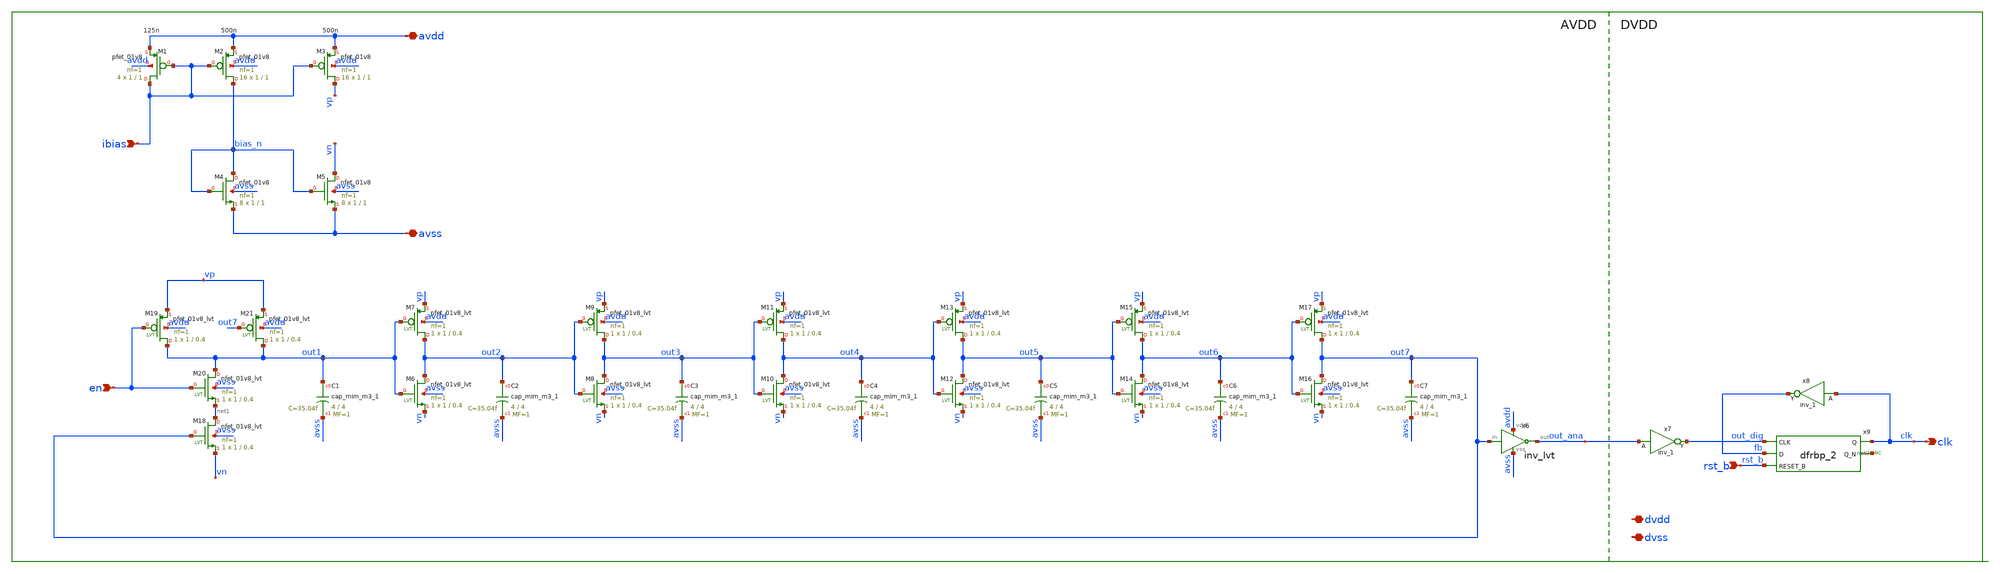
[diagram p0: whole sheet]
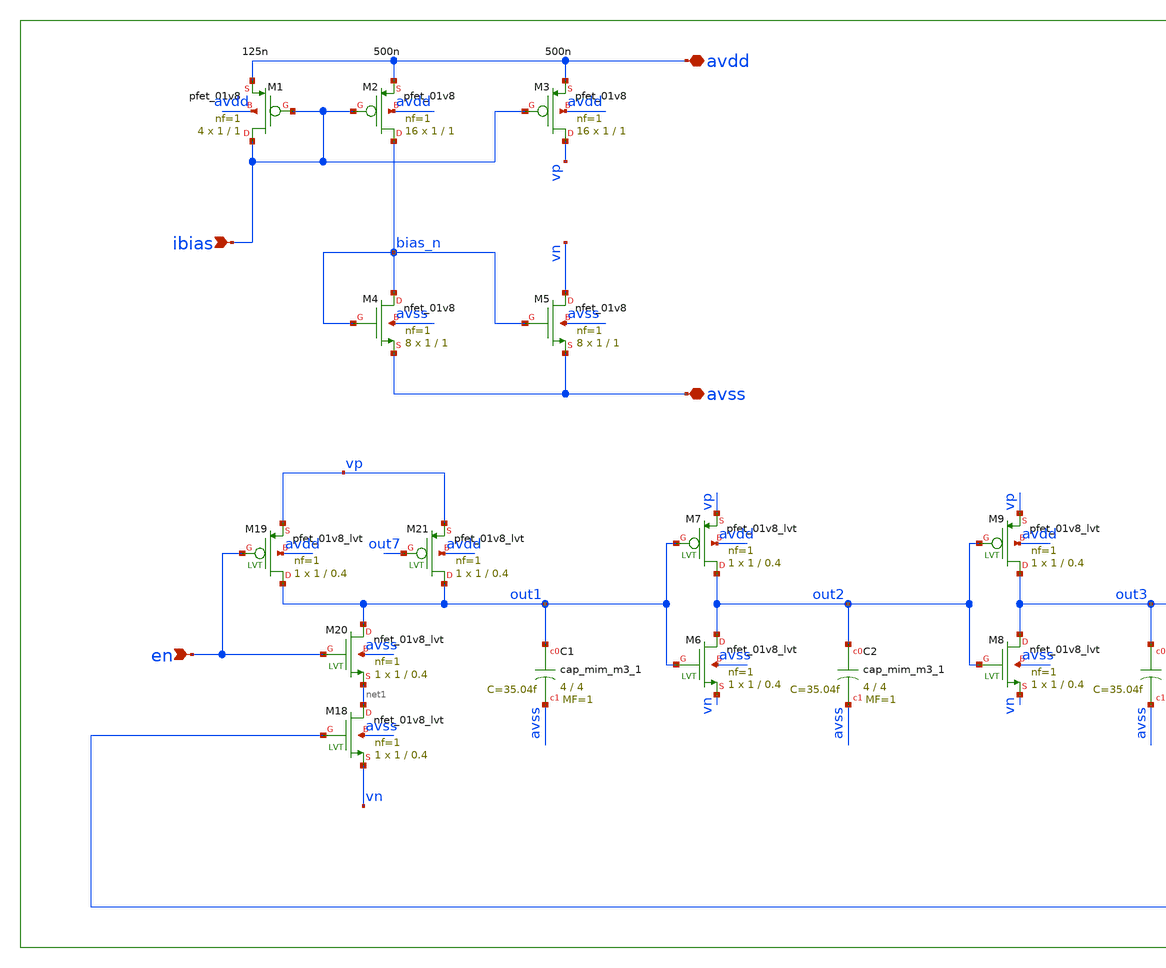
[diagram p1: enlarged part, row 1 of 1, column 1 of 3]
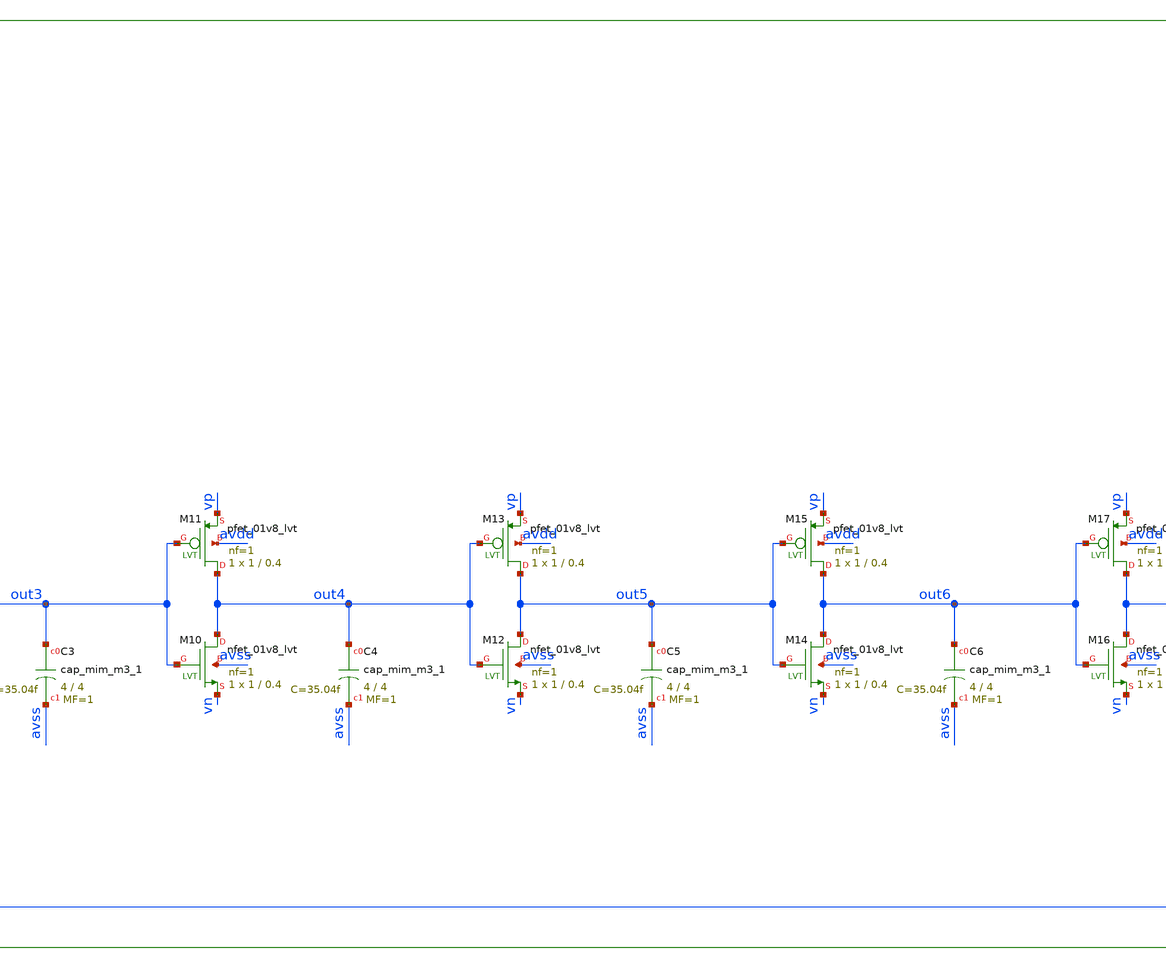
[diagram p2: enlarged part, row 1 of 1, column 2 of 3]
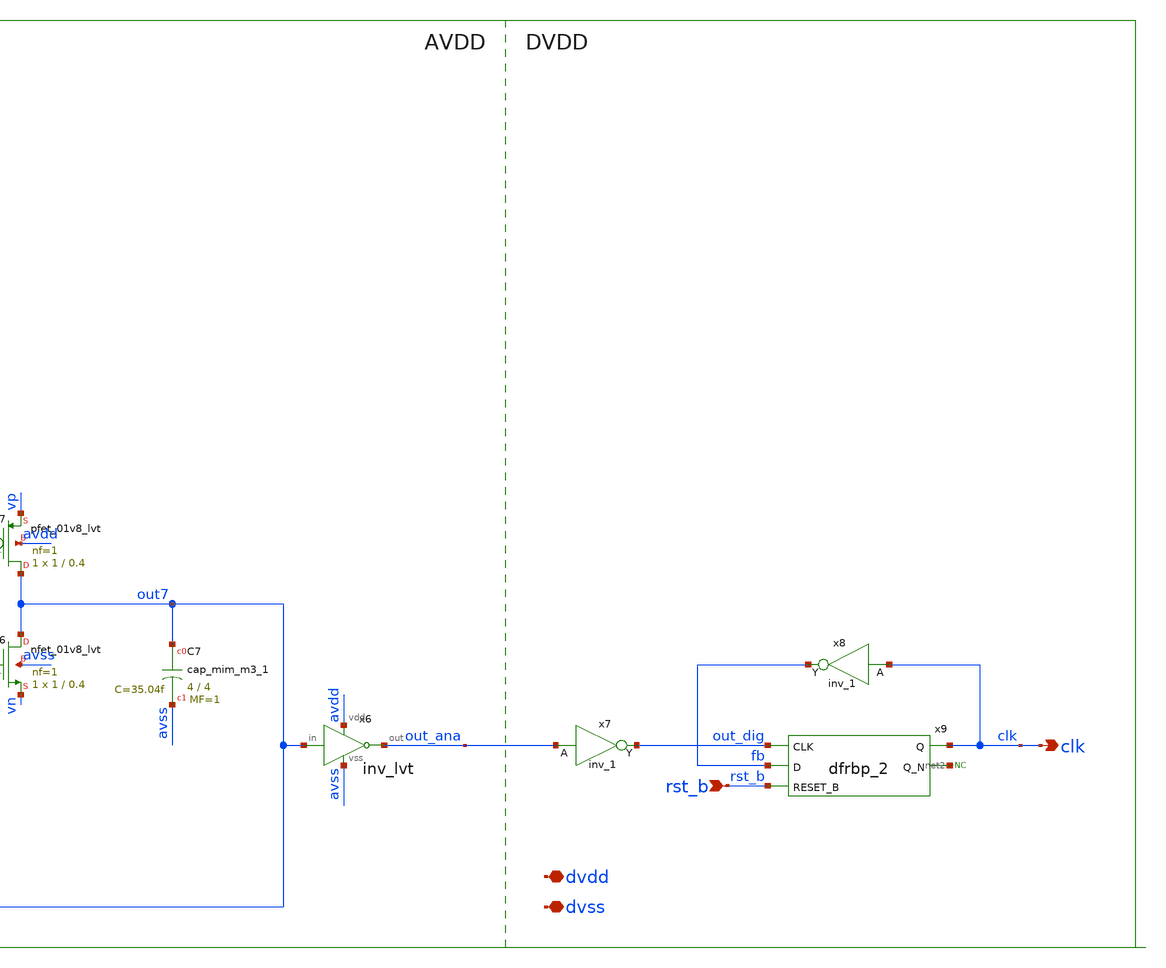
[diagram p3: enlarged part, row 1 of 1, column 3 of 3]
** sch_path: xschem/rosc/rosc.sch
**.subckt rosc en avss clk dvdd dvss avdd rst_b ibias
*.ipin en
*.iopin avss
*.opin clk
*.iopin dvdd
*.iopin dvss
*.iopin avdd
*.ipin rst_b
*.ipin ibias
x8 clk dvss dvss dvdd dvdd fb sky130_fd_sc_hd__inv_1
* noconn #net2
XM2 bias_n ibias avdd avdd sky130_fd_pr__pfet_01v8 L=1 W=1 nf=1 ad='int((nf+1)/2) * W/nf * 0.29' as='int((nf+2)/2) * W/nf * 0.29'
+ pd='2*int((nf+1)/2) * (W/nf + 0.29)' ps='2*int((nf+2)/2) * (W/nf + 0.29)' nrd='0.29 / W' nrs='0.29 / W'
+ sa=0 sb=0 sd=0 mult=16 m=16
XM1 ibias ibias avdd avdd sky130_fd_pr__pfet_01v8 L=1 W=1 nf=1 ad='int((nf+1)/2) * W/nf * 0.29' as='int((nf+2)/2) * W/nf * 0.29'
+ pd='2*int((nf+1)/2) * (W/nf + 0.29)' ps='2*int((nf+2)/2) * (W/nf + 0.29)' nrd='0.29 / W' nrs='0.29 / W'
+ sa=0 sb=0 sd=0 mult=4 m=4
x9 out_dig fb rst_b dvss dvss dvdd dvdd clk net2 sky130_fd_sc_hd__dfrbp_2
XM4 bias_n bias_n avss avss sky130_fd_pr__nfet_01v8 L=1 W=1 nf=1 ad='int((nf+1)/2) * W/nf * 0.29' as='int((nf+2)/2) * W/nf * 0.29'
+ pd='2*int((nf+1)/2) * (W/nf + 0.29)' ps='2*int((nf+2)/2) * (W/nf + 0.29)' nrd='0.29 / W' nrs='0.29 / W'
+ sa=0 sb=0 sd=0 mult=8 m=8
XM5 vn bias_n avss avss sky130_fd_pr__nfet_01v8 L=1 W=1 nf=1 ad='int((nf+1)/2) * W/nf * 0.29' as='int((nf+2)/2) * W/nf * 0.29'
+ pd='2*int((nf+1)/2) * (W/nf + 0.29)' ps='2*int((nf+2)/2) * (W/nf + 0.29)' nrd='0.29 / W' nrs='0.29 / W'
+ sa=0 sb=0 sd=0 mult=8 m=8
x7 out_ana dvss dvss dvdd dvdd out_dig sky130_fd_sc_hd__inv_1
XM3 vp ibias avdd avdd sky130_fd_pr__pfet_01v8 L=1 W=1 nf=1 ad='int((nf+1)/2) * W/nf * 0.29' as='int((nf+2)/2) * W/nf * 0.29'
+ pd='2*int((nf+1)/2) * (W/nf + 0.29)' ps='2*int((nf+2)/2) * (W/nf + 0.29)' nrd='0.29 / W' nrs='0.29 / W'
+ sa=0 sb=0 sd=0 mult=16 m=16
XC1 out1 avss sky130_fd_pr__cap_mim_m3_1 W=4 L=4 MF=1 m=1
XC2 out2 avss sky130_fd_pr__cap_mim_m3_1 W=4 L=4 MF=1 m=1
x6 avdd out7 out_ana avss inv_lvt
XM6 out2 out1 vn avss sky130_fd_pr__nfet_01v8_lvt L=0.4 W=1 nf=1 ad='int((nf+1)/2) * W/nf * 0.29' as='int((nf+2)/2) * W/nf * 0.29'
+ pd='2*int((nf+1)/2) * (W/nf + 0.29)' ps='2*int((nf+2)/2) * (W/nf + 0.29)' nrd='0.29 / W' nrs='0.29 / W'
+ sa=0 sb=0 sd=0 mult=1 m=1
XM7 out2 out1 vp avdd sky130_fd_pr__pfet_01v8_lvt L=0.4 W=1 nf=1 ad='int((nf+1)/2) * W/nf * 0.29' as='int((nf+2)/2) * W/nf * 0.29'
+ pd='2*int((nf+1)/2) * (W/nf + 0.29)' ps='2*int((nf+2)/2) * (W/nf + 0.29)' nrd='0.29 / W' nrs='0.29 / W'
+ sa=0 sb=0 sd=0 mult=1 m=1
XC3 out3 avss sky130_fd_pr__cap_mim_m3_1 W=4 L=4 MF=1 m=1
XC4 out4 avss sky130_fd_pr__cap_mim_m3_1 W=4 L=4 MF=1 m=1
XC5 out5 avss sky130_fd_pr__cap_mim_m3_1 W=4 L=4 MF=1 m=1
XC6 out6 avss sky130_fd_pr__cap_mim_m3_1 W=4 L=4 MF=1 m=1
XM18 net1 out7 vn avss sky130_fd_pr__nfet_01v8_lvt L=0.4 W=1 nf=1 ad='int((nf+1)/2) * W/nf * 0.29' as='int((nf+2)/2) * W/nf * 0.29'
+ pd='2*int((nf+1)/2) * (W/nf + 0.29)' ps='2*int((nf+2)/2) * (W/nf + 0.29)' nrd='0.29 / W' nrs='0.29 / W'
+ sa=0 sb=0 sd=0 mult=1 m=1
XM19 out1 en vp avdd sky130_fd_pr__pfet_01v8_lvt L=0.4 W=1 nf=1 ad='int((nf+1)/2) * W/nf * 0.29' as='int((nf+2)/2) * W/nf * 0.29'
+ pd='2*int((nf+1)/2) * (W/nf + 0.29)' ps='2*int((nf+2)/2) * (W/nf + 0.29)' nrd='0.29 / W' nrs='0.29 / W'
+ sa=0 sb=0 sd=0 mult=1 m=1
XM20 out1 en net1 avss sky130_fd_pr__nfet_01v8_lvt L=0.4 W=1 nf=1 ad='int((nf+1)/2) * W/nf * 0.29' as='int((nf+2)/2) * W/nf * 0.29'
+ pd='2*int((nf+1)/2) * (W/nf + 0.29)' ps='2*int((nf+2)/2) * (W/nf + 0.29)' nrd='0.29 / W' nrs='0.29 / W'
+ sa=0 sb=0 sd=0 mult=1 m=1
XM21 out1 out7 vp avdd sky130_fd_pr__pfet_01v8_lvt L=0.4 W=1 nf=1 ad='int((nf+1)/2) * W/nf * 0.29' as='int((nf+2)/2) * W/nf * 0.29'
+ pd='2*int((nf+1)/2) * (W/nf + 0.29)' ps='2*int((nf+2)/2) * (W/nf + 0.29)' nrd='0.29 / W' nrs='0.29 / W'
+ sa=0 sb=0 sd=0 mult=1 m=1
XM8 out3 out2 vn avss sky130_fd_pr__nfet_01v8_lvt L=0.4 W=1 nf=1 ad='int((nf+1)/2) * W/nf * 0.29' as='int((nf+2)/2) * W/nf * 0.29'
+ pd='2*int((nf+1)/2) * (W/nf + 0.29)' ps='2*int((nf+2)/2) * (W/nf + 0.29)' nrd='0.29 / W' nrs='0.29 / W'
+ sa=0 sb=0 sd=0 mult=1 m=1
XM9 out3 out2 vp avdd sky130_fd_pr__pfet_01v8_lvt L=0.4 W=1 nf=1 ad='int((nf+1)/2) * W/nf * 0.29' as='int((nf+2)/2) * W/nf * 0.29'
+ pd='2*int((nf+1)/2) * (W/nf + 0.29)' ps='2*int((nf+2)/2) * (W/nf + 0.29)' nrd='0.29 / W' nrs='0.29 / W'
+ sa=0 sb=0 sd=0 mult=1 m=1
XM10 out4 out3 vn avss sky130_fd_pr__nfet_01v8_lvt L=0.4 W=1 nf=1 ad='int((nf+1)/2) * W/nf * 0.29' as='int((nf+2)/2) * W/nf * 0.29'
+ pd='2*int((nf+1)/2) * (W/nf + 0.29)' ps='2*int((nf+2)/2) * (W/nf + 0.29)' nrd='0.29 / W' nrs='0.29 / W'
+ sa=0 sb=0 sd=0 mult=1 m=1
XM11 out4 out3 vp avdd sky130_fd_pr__pfet_01v8_lvt L=0.4 W=1 nf=1 ad='int((nf+1)/2) * W/nf * 0.29' as='int((nf+2)/2) * W/nf * 0.29'
+ pd='2*int((nf+1)/2) * (W/nf + 0.29)' ps='2*int((nf+2)/2) * (W/nf + 0.29)' nrd='0.29 / W' nrs='0.29 / W'
+ sa=0 sb=0 sd=0 mult=1 m=1
XM12 out5 out4 vn avss sky130_fd_pr__nfet_01v8_lvt L=0.4 W=1 nf=1 ad='int((nf+1)/2) * W/nf * 0.29' as='int((nf+2)/2) * W/nf * 0.29'
+ pd='2*int((nf+1)/2) * (W/nf + 0.29)' ps='2*int((nf+2)/2) * (W/nf + 0.29)' nrd='0.29 / W' nrs='0.29 / W'
+ sa=0 sb=0 sd=0 mult=1 m=1
XM13 out5 out4 vp avdd sky130_fd_pr__pfet_01v8_lvt L=0.4 W=1 nf=1 ad='int((nf+1)/2) * W/nf * 0.29' as='int((nf+2)/2) * W/nf * 0.29'
+ pd='2*int((nf+1)/2) * (W/nf + 0.29)' ps='2*int((nf+2)/2) * (W/nf + 0.29)' nrd='0.29 / W' nrs='0.29 / W'
+ sa=0 sb=0 sd=0 mult=1 m=1
XM14 out6 out5 vn avss sky130_fd_pr__nfet_01v8_lvt L=0.4 W=1 nf=1 ad='int((nf+1)/2) * W/nf * 0.29' as='int((nf+2)/2) * W/nf * 0.29'
+ pd='2*int((nf+1)/2) * (W/nf + 0.29)' ps='2*int((nf+2)/2) * (W/nf + 0.29)' nrd='0.29 / W' nrs='0.29 / W'
+ sa=0 sb=0 sd=0 mult=1 m=1
XM15 out6 out5 vp avdd sky130_fd_pr__pfet_01v8_lvt L=0.4 W=1 nf=1 ad='int((nf+1)/2) * W/nf * 0.29' as='int((nf+2)/2) * W/nf * 0.29'
+ pd='2*int((nf+1)/2) * (W/nf + 0.29)' ps='2*int((nf+2)/2) * (W/nf + 0.29)' nrd='0.29 / W' nrs='0.29 / W'
+ sa=0 sb=0 sd=0 mult=1 m=1
XM16 out7 out6 vn avss sky130_fd_pr__nfet_01v8_lvt L=0.4 W=1 nf=1 ad='int((nf+1)/2) * W/nf * 0.29' as='int((nf+2)/2) * W/nf * 0.29'
+ pd='2*int((nf+1)/2) * (W/nf + 0.29)' ps='2*int((nf+2)/2) * (W/nf + 0.29)' nrd='0.29 / W' nrs='0.29 / W'
+ sa=0 sb=0 sd=0 mult=1 m=1
XM17 out7 out6 vp avdd sky130_fd_pr__pfet_01v8_lvt L=0.4 W=1 nf=1 ad='int((nf+1)/2) * W/nf * 0.29' as='int((nf+2)/2) * W/nf * 0.29'
+ pd='2*int((nf+1)/2) * (W/nf + 0.29)' ps='2*int((nf+2)/2) * (W/nf + 0.29)' nrd='0.29 / W' nrs='0.29 / W'
+ sa=0 sb=0 sd=0 mult=1 m=1
XC7 out7 avss sky130_fd_pr__cap_mim_m3_1 W=4 L=4 MF=1 m=1
**.ends

* expanding   symbol:  logic/inv_lvt.sym # of pins=4
** sym_path: xschem/logic/inv_lvt.sym
** sch_path: xschem/logic/inv_lvt.sch
.subckt inv_lvt vdd in out vss
*.iopin vdd
*.iopin vss
*.ipin in
*.opin out
XM1 out in vss vss sky130_fd_pr__nfet_01v8_lvt L=0.4 W=1 nf=1 ad='int((nf+1)/2) * W/nf * 0.29' as='int((nf+2)/2) * W/nf * 0.29'
+ pd='2*int((nf+1)/2) * (W/nf + 0.29)' ps='2*int((nf+2)/2) * (W/nf + 0.29)' nrd='0.29 / W' nrs='0.29 / W'
+ sa=0 sb=0 sd=0 mult=1 m=1
XM2 out in vdd vdd sky130_fd_pr__pfet_01v8_lvt L=0.4 W=1 nf=1 ad='int((nf+1)/2) * W/nf * 0.29' as='int((nf+2)/2) * W/nf * 0.29'
+ pd='2*int((nf+1)/2) * (W/nf + 0.29)' ps='2*int((nf+2)/2) * (W/nf + 0.29)' nrd='0.29 / W' nrs='0.29 / W'
+ sa=0 sb=0 sd=0 mult=1 m=1
.ends

.end
